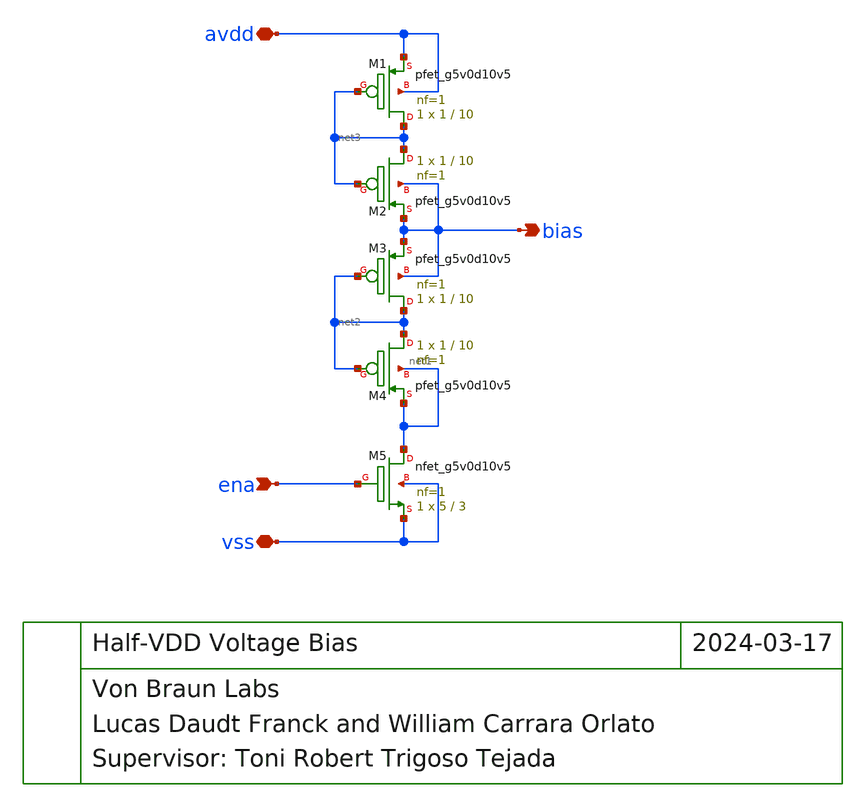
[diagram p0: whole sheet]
** sch_path: blocks/input/xschem/halfvdd_vbias.sch
**.subckt halfvdd_vbias ena vss avdd bias
*.ipin ena
*.iopin vss
*.iopin avdd
*.opin bias
XM1 net3 net3 avdd avdd sky130_fd_pr__pfet_g5v0d10v5 L=10 W=1 nf=1 ad='int((nf+1)/2) * W/nf * 0.29' as='int((nf+2)/2) * W/nf * 0.29'
+ pd='2*int((nf+1)/2) * (W/nf + 0.29)' ps='2*int((nf+2)/2) * (W/nf + 0.29)' nrd='0.29 / W' nrs='0.29 / W'
+ sa=0 sb=0 sd=0 mult=1 m=1
XM2 net3 net3 bias bias sky130_fd_pr__pfet_g5v0d10v5 L=10 W=1 nf=1 ad='int((nf+1)/2) * W/nf * 0.29' as='int((nf+2)/2) * W/nf * 0.29'
+ pd='2*int((nf+1)/2) * (W/nf + 0.29)' ps='2*int((nf+2)/2) * (W/nf + 0.29)' nrd='0.29 / W' nrs='0.29 / W'
+ sa=0 sb=0 sd=0 mult=1 m=1
XM3 net2 net2 bias bias sky130_fd_pr__pfet_g5v0d10v5 L=10 W=1 nf=1 ad='int((nf+1)/2) * W/nf * 0.29' as='int((nf+2)/2) * W/nf * 0.29'
+ pd='2*int((nf+1)/2) * (W/nf + 0.29)' ps='2*int((nf+2)/2) * (W/nf + 0.29)' nrd='0.29 / W' nrs='0.29 / W'
+ sa=0 sb=0 sd=0 mult=1 m=1
XM4 net2 net2 net1 net1 sky130_fd_pr__pfet_g5v0d10v5 L=10 W=1 nf=1 ad='int((nf+1)/2) * W/nf * 0.29' as='int((nf+2)/2) * W/nf * 0.29'
+ pd='2*int((nf+1)/2) * (W/nf + 0.29)' ps='2*int((nf+2)/2) * (W/nf + 0.29)' nrd='0.29 / W' nrs='0.29 / W'
+ sa=0 sb=0 sd=0 mult=1 m=1
XM5 net1 ena vss vss sky130_fd_pr__nfet_g5v0d10v5 L=3 W=5 nf=1 ad='int((nf+1)/2) * W/nf * 0.29' as='int((nf+2)/2) * W/nf * 0.29'
+ pd='2*int((nf+1)/2) * (W/nf + 0.29)' ps='2*int((nf+2)/2) * (W/nf + 0.29)' nrd='0.29 / W' nrs='0.29 / W'
+ sa=0 sb=0 sd=0 mult=1 m=1
**.ends
.end
